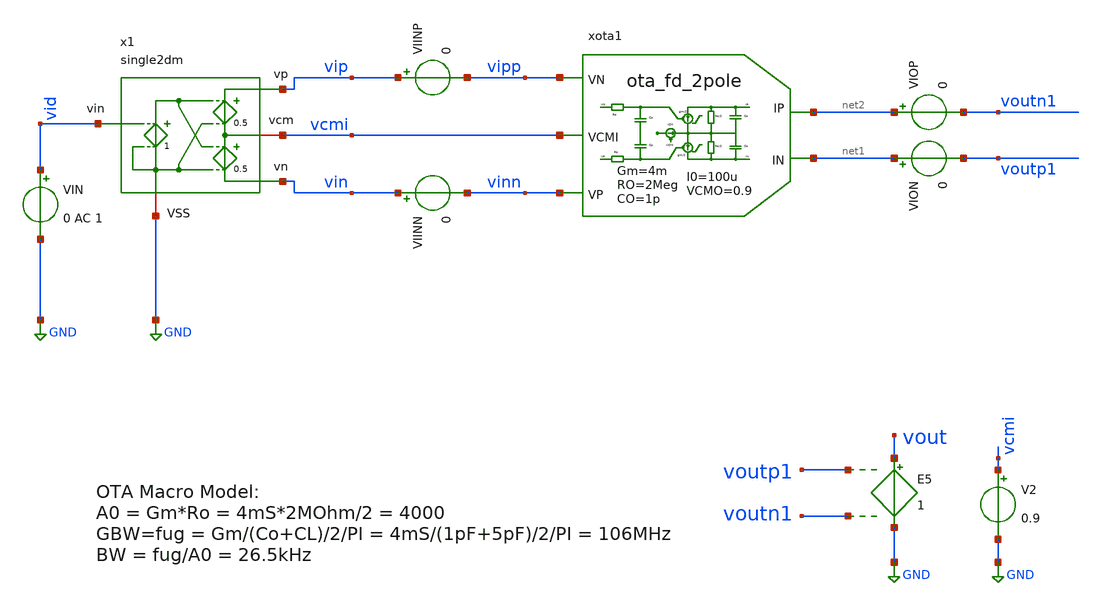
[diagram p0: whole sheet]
** sch_path: macros/filter_cmos5l/testbenches/xschem/ota_fd_2pole_tb.sch
**.subckt ota_fd_2pole_tb
V2 vcmi GND 0.9
VIN vid GND 0 AC 1
VIINP vip vipp 0
VIINN vin vinn 0
E5 vout GND voutp1 voutn1 1
VIOP net2 voutn1 0
VION net1 voutp1 0
xota1 vipp net2 net1 vinn vcmi ota_fd_2pole GM=4m RO=2Meg CO=1p RP=0 CP=0.1p VCMO=0.9 I0=100u
x1 vip vid vcmi GND vin single2dm
**** begin user architecture code


.options savecurrents
.options method=gear reltol=.005
.options sparse
.control
save all

let f_sig = 100
let f_min = 10
let f_max = 1000Meg
let f_stop = 5Meg
let tper_sig = 1/f_sig
let tfr_sig = tper_sig/2
let Adc = 4000
let v_step_o = 0.9
let v_step_i = v_step_o/Adc

let t_rf = 0.1u
let t_step = 50u
let t_delay = 0
let t_per = 2*t_step

let tstep = 0.1*t_rf
let tstop = 2*t_per
let tstart = t_delay

alter @VIN[PULSE] = [ 0 $&v_step_i $&t_delay $&t_rf $&t_rf $&t_step $&t_per 0 ]

set wr_singlescale
set wr_vecnames
option numdgt=3


** Main Simulations
	op
	ac dec 100 $&const.f_min $&const.f_max
	tran $&tstep $&tstop $&tstart

	setplot ac1
	let A = v(vout)/v(vid)

	let Amag_dB = vdb(A)
	settype decibel Amag_dB
	let Aarg = 180/PI*cphase(A)

	let fdc = const.f_min+1
	meas ac Adc find Amag_dB when frequency = fdc
	let Amag_fc = Adc-3
	meas ac fc find frequency when Amag_dB = Amag_fc
	meas ac Amax max Amag_dB
	meas ac fug find frequency when Amag_dB=0

	let Adc_lin = 10^(Adc/20)
	let GBW = Adc_lin*fc
	print Adc_lin
	print GBW

	plot Amag_dB Aarg ylabel 'Magnitude, Phase'

	setplot tran1
	let vid = v(vid)
	let iop = viop#branch
	let ion = vion#branch
	let vcmo = (voutp1+voutn1)/2

	*plot iop ion
	plot vid vout vcmo
	plot v(vip) v(vin) v(voutp1) v(voutn1) vcmo


alter @VIN[DC] = 0
op

remzerovec
write ota_fd_2pole_tb.raw
.endc

**** end user architecture code
**.ends

* expanding   symbol:  ota_fd_2pole.sym # of pins=5
** sym_path: ota_fd_2pole.sym
** sch_path: ota_fd_2pole.sch
.subckt ota_fd_2pole VN IP IN VP VCMI  GM=1u RO=100Meg CO=1p RP=0 CP=0.1p VCMO=0 I0=1u
*.ipin VP
*.ipin VN
*.opin IP
*.opin IN
*.ipin VCMI
R3 IP net1 {RO/2} m=1
R4 IN net1 {RO/2} m=1
C3 IP net1 {CO} m=1
R5 VN ip1 {RP} m=1
C4 ip1 VCMI {CP} m=1
C6 in1 VCMI {CP} m=1
C8 IN net1 {CO} m=1
R7 VP in1 {RP} m=1
B2 IP net1 I = {I0*tanh(GM/2*V(ip1,in1)/I0)}
B1 net1 IN I = {I0*tanh(GM/2*V(ip1,in1)/I0)}
B5 net1 GND I = {VCMO-(V(IP)+V(IN))/2}
.ends


* expanding   symbol:  single2dm.sym # of pins=5
** sym_path: single2dm.sym
** sch_path: single2dm.sch
.subckt single2dm vp vin vcm VSS vn
*.ipin vin
*.opin vn
*.iopin vcm
*.opin vp
*.iopin VSS
E3 vcm vn net1 VSS 0.5
E2 vp vcm net1 VSS 0.5
E1 net1 VSS vin VSS 1
.ends

.GLOBAL GND
.end
